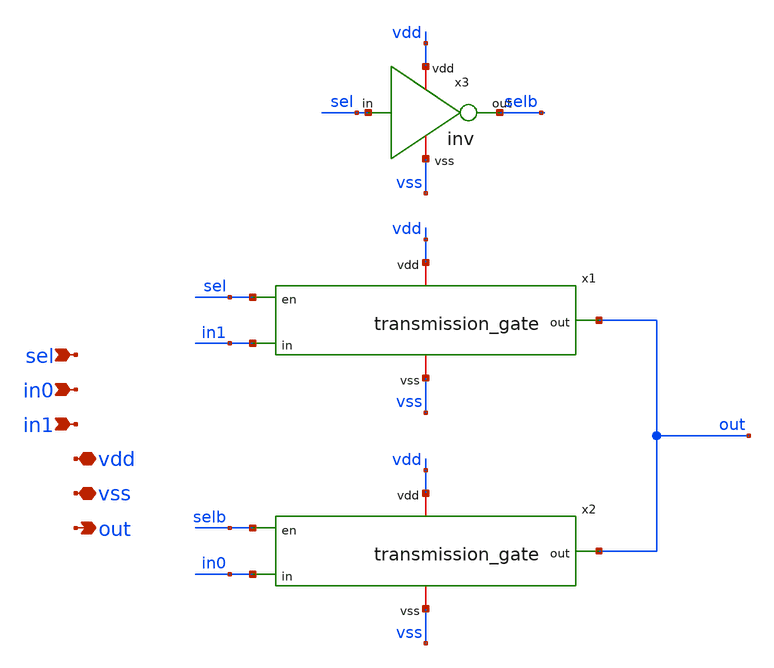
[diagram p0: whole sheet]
** sch_path: DESIGN/DACFUTURE_EDU/analog_mux/analog_mux.sch
**.subckt analog_mux sel in0 in1 vdd vss out
*.ipin sel
*.ipin in0
*.ipin in1
*.iopin vdd
*.iopin vss
*.opin out
x1 vdd vss sel in1 out transmission_gate
x2 vdd vss selb in0 out transmission_gate
x3 sel selb vdd vss inv
**.ends
.end
